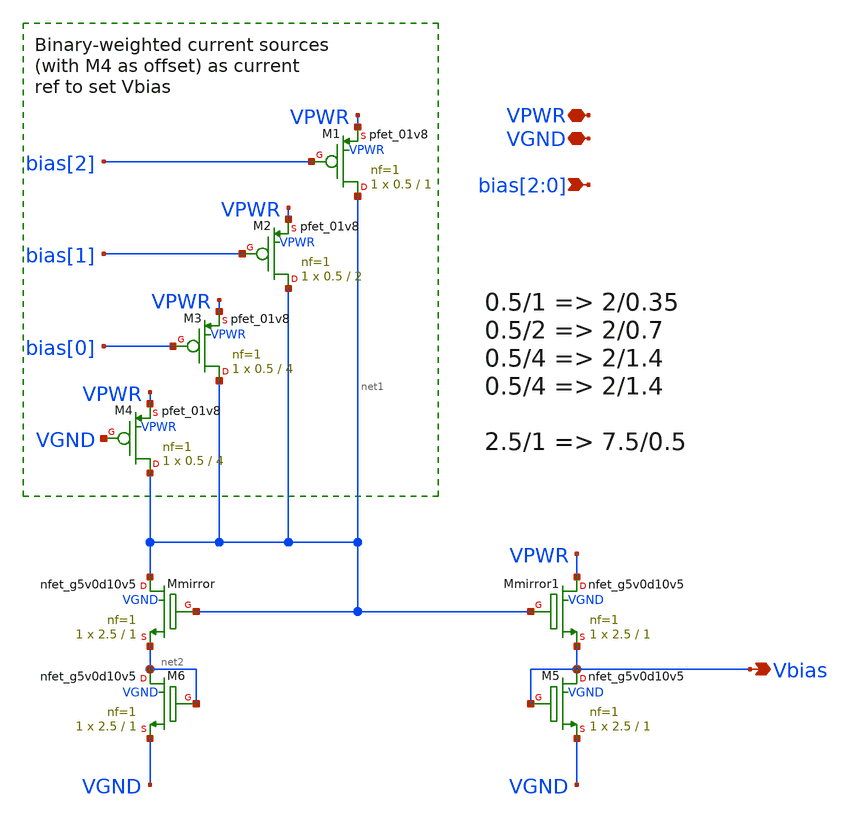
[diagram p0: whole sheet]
** sch_path: xschem-cascode-backup/vbiasPFET.sch
**.subckt vbiasPFET VPWR VGND bias[2],bias[1],bias[0] Vbias
*.iopin VPWR
*.iopin VGND
*.ipin bias[2],bias[1],bias[0]
*.opin Vbias
XM1 net1 bias[2] VPWR VPWR sky130_fd_pr__pfet_01v8 L=1 W=0.5 nf=1 ad='int((nf+1)/2) * W/nf * 0.29' as='int((nf+2)/2) * W/nf * 0.29'
+ pd='2*int((nf+1)/2) * (W/nf + 0.29)' ps='2*int((nf+2)/2) * (W/nf + 0.29)' nrd='0.29 / W' nrs='0.29 / W'
+ sa=0 sb=0 sd=0 mult=1 m=1
XM2 net1 bias[1] VPWR VPWR sky130_fd_pr__pfet_01v8 L=2 W=0.5 nf=1 ad='int((nf+1)/2) * W/nf * 0.29' as='int((nf+2)/2) * W/nf * 0.29'
+ pd='2*int((nf+1)/2) * (W/nf + 0.29)' ps='2*int((nf+2)/2) * (W/nf + 0.29)' nrd='0.29 / W' nrs='0.29 / W'
+ sa=0 sb=0 sd=0 mult=1 m=1
XM3 net1 bias[0] VPWR VPWR sky130_fd_pr__pfet_01v8 L=4 W=0.5 nf=1 ad='int((nf+1)/2) * W/nf * 0.29' as='int((nf+2)/2) * W/nf * 0.29'
+ pd='2*int((nf+1)/2) * (W/nf + 0.29)' ps='2*int((nf+2)/2) * (W/nf + 0.29)' nrd='0.29 / W' nrs='0.29 / W'
+ sa=0 sb=0 sd=0 mult=1 m=1
XM4 net1 VGND VPWR VPWR sky130_fd_pr__pfet_01v8 L=4 W=0.5 nf=1 ad='int((nf+1)/2) * W/nf * 0.29' as='int((nf+2)/2) * W/nf * 0.29'
+ pd='2*int((nf+1)/2) * (W/nf + 0.29)' ps='2*int((nf+2)/2) * (W/nf + 0.29)' nrd='0.29 / W' nrs='0.29 / W'
+ sa=0 sb=0 sd=0 mult=1 m=1
XM6 net2 net2 VGND VGND sky130_fd_pr__nfet_g5v0d10v5 L=1 W=2.5 nf=1 ad='int((nf+1)/2) * W/nf * 0.29'
+ as='int((nf+2)/2) * W/nf * 0.29' pd='2*int((nf+1)/2) * (W/nf + 0.29)' ps='2*int((nf+2)/2) * (W/nf + 0.29)'
+ nrd='0.29 / W' nrs='0.29 / W' sa=0 sb=0 sd=0 mult=1 m=1
XMmirror net1 net1 net2 VGND sky130_fd_pr__nfet_g5v0d10v5 L=1 W=2.5 nf=1 ad='int((nf+1)/2) * W/nf * 0.29'
+ as='int((nf+2)/2) * W/nf * 0.29' pd='2*int((nf+1)/2) * (W/nf + 0.29)' ps='2*int((nf+2)/2) * (W/nf + 0.29)'
+ nrd='0.29 / W' nrs='0.29 / W' sa=0 sb=0 sd=0 mult=1 m=1
XM5 Vbias Vbias VGND VGND sky130_fd_pr__nfet_g5v0d10v5 L=1 W=2.5 nf=1 ad='int((nf+1)/2) * W/nf * 0.29'
+ as='int((nf+2)/2) * W/nf * 0.29' pd='2*int((nf+1)/2) * (W/nf + 0.29)' ps='2*int((nf+2)/2) * (W/nf + 0.29)'
+ nrd='0.29 / W' nrs='0.29 / W' sa=0 sb=0 sd=0 mult=1 m=1
XMmirror1 VPWR net1 Vbias VGND sky130_fd_pr__nfet_g5v0d10v5 L=1 W=2.5 nf=1 ad='int((nf+1)/2) * W/nf * 0.29'
+ as='int((nf+2)/2) * W/nf * 0.29' pd='2*int((nf+1)/2) * (W/nf + 0.29)' ps='2*int((nf+2)/2) * (W/nf + 0.29)'
+ nrd='0.29 / W' nrs='0.29 / W' sa=0 sb=0 sd=0 mult=1 m=1
**.ends
.end
